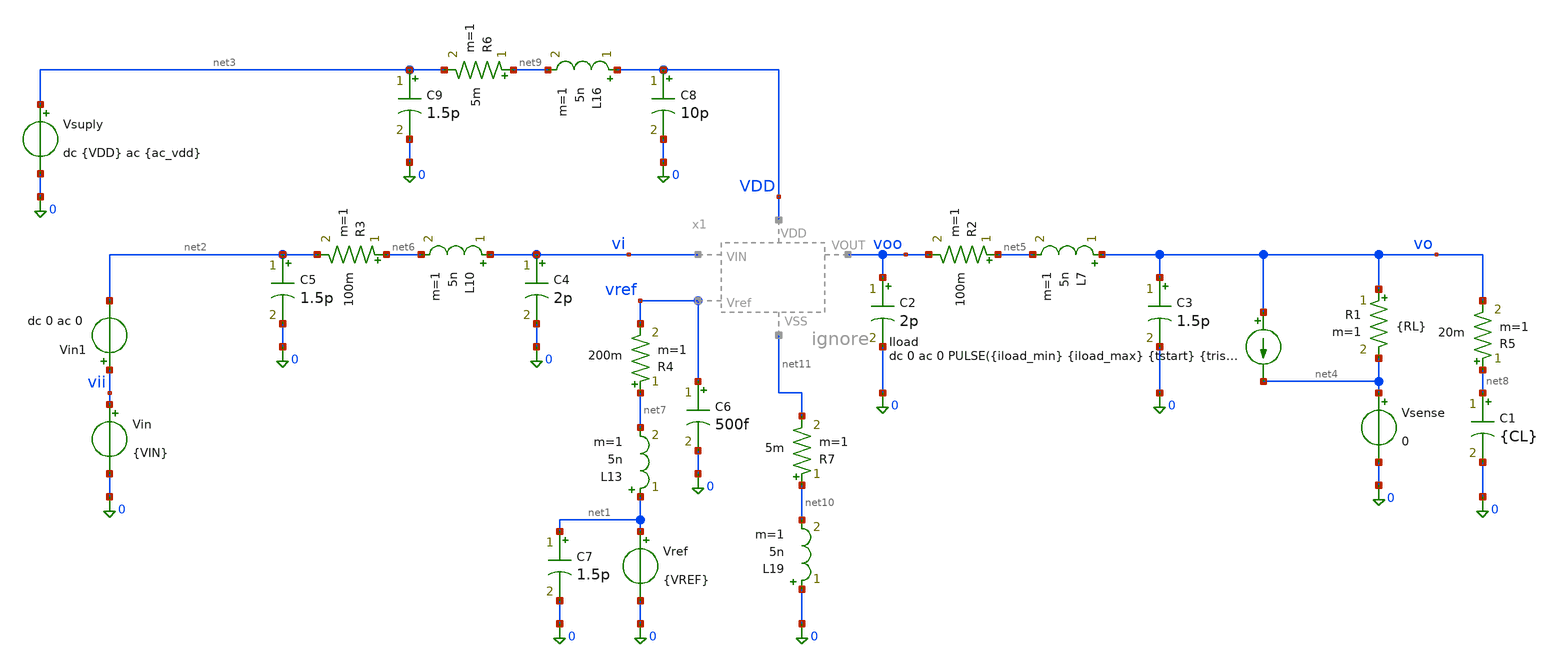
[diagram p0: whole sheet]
** sch_path: xschem/LDO_Top/ldo_tb_pex_montecarlo.sch
**.subckt ldo_tb_pex_montecarlo
Vsuply net3 0 dc {VDD} ac {ac_vdd}
Vref net1 0 {VREF}
Vin vii 0 {VIN}
R1 vo net4 {RL} m=1
C1 net8 0 {CL} m=1
Iload vo net4 dc 0 ac 0 PULSE({iload_min} {iload_max} {tstart} {trise} {tfall} {twidth} {tperiod})
Vsense net4 0 0
Vin1 vii net2 dc 0 ac 0
C2 voo 0 2p m=1
R2 net5 voo 100m m=1
L7 vo net5 5n m=1
C3 vo 0 1.5p m=1
L10 vi net6 5n m=1
C4 vi 0 2p m=1
C5 net2 0 1.5p m=1
R3 net6 net2 100m m=1
L13 net1 net7 5n m=1
R4 net7 vref 200m m=1
C6 vref 0 500f m=1
C7 net1 0 1.5p m=1
R5 net8 vo 20m m=1
L16 VDD net9 5n m=1
C8 VDD 0 10p m=1
C9 net3 0 1.5p m=1
R6 net9 net3 5m m=1
L19 0 net10 5n m=1
R7 net10 net11 5m m=1
**** begin user architecture code


* ==============================================================================
* ENCABEZADO DEL ARCHIVO (ldo_tb_pex_montecarlo.sch):
* Descripción:
*   Banco de pruebas Monte Carlo Post-Layout (PEX) para el regulador LDO
*   completo (incluyendo LDO_pex.spice), incorporando los modelos parásitos de
*   inductancia, resistencia y capacitancia de línea/empaquetado en todos los
*   pines (VIN, VOUT, VDD, Vref, VSS) y la ESR del capacitor de salida.
*   Evalúa Overshoot/Undershoot, PSRR, Line Regulation, Load Regulation y
*   Dropout en cada iteración y guarda en 'datos_mc.txt' con el formato exacto
*   que lee el notebook 'LDO_tb_montecarlo.ipynb'.
* ==============================================================================

* 1. Librería de modelos Sky130 con Mismatch (tt_mm) y netlist PEX del LDO
.lib /foss/pdks/sky130A/libs.tech/ngspice/sky130.lib.spice tt_mm
.include /foss/designs/LDO-sky130/xschem/LDO_Top/LDO_pex.spice
x1 vi voo VDD vref net11 LDO

.option temp=27
.option num_threads=8
.option gmin=1e-12 reltol=1e-3 abstol=1e-12 vntol=1e-6 itl1=500 itl2=200 itl4=100

.param rsh_var = agauss(0, 0.005, 1)

* Guardar únicamente los nodos clave para no desbordar la RAM con la red RC parásita
.save v(vo) v(voo) v(vi) v(vii) v(vdd) v(vref) v(x1.OTA_0.VO_ota) v(x1.OTA_0.VIP_ota) v(x1.self_bias_0.VR)

* Condiciones iniciales en los nodos reales de LDO_pex.spice para convergencia DC
.nodeset V(vo)=1.2
.nodeset V(voo)=1.2
.nodeset V(x1.OTA_0.VIP_ota)=0.6
.nodeset V(x1.OTA_0.VO_ota)=1.1
.nodeset V(x1.self_bias_0.VR)=0.6
.nodeset V(x1.self_bias_0.vgp_self)=1.0

* Parámetros nominales del LDO
.param VDD = 1.8
.param VREF = 0.6
.param VIN = '1*VDD-0.3'
.param RL = 240e9
.param CL = 1u

* Parámetros para la prueba transitoria de carga (Overshoot / Undershoot)
.param iload_min = 1u
.param iload_max = 5m
.param tstart   = 30u
.param trise    = 100n
.param tfall    = 100n
.param twidth   = 100u
.param tperiod  = 200u
.param tsim     = '2*tperiod'

.param ac_iprobe = 0
.param ac_vdd    = 0

* --- Clamp SOLO de simulación (evita soluciones DC falsas en los nodos reales del PEX) ---
Dclpn 0 vo dclamp_tb
Dclpp vo vclp dclamp_tb
Dclpn2 0 x1.OTA_0.VIP_ota dclamp_tb
Dclpp2 x1.OTA_0.VIP_ota vclp dclamp_tb
Vclp vclp 0 5
.model dclamp_tb D(IS=1e-15 N=1)

.control
* =========================================================
* CONFIGURACION DEL BUCLE MONTE CARLO PEX
* =========================================================
let mc_runs = 100
let run = 1

set appendwrite
set filetype=ascii

let tperiod = 200u
let tsim = 2 * tperiod

echo === INICIO MONTE CARLO PEX === > datos_mc.txt

* =========================================================
* INICIO DEL BUCLE MONTE CARLO PEX
* =========================================================
while run <= mc_runs

    echo ======================================
    echo CORRIENDO MONTE CARLO PEX ITERACION: $&run
    echo ======================================
    echo --- ITERACION: $&run --- >> datos_mc.txt

    * En la iteración 1 el circuito ya fue cargado con su primera semilla;
    * a partir de la iteración 2 hacemos UN SOLO 'reset' por chip para
    * sortear nuevos parámetros estadísticos (agauss) y restaurar las fuentes.
    if run > 1
        reset
    end

    save v(vo) v(vi) v(vdd)

    * -----------------------------------------------------
    * A. TRANSIENTE (Overshoot y Undershoot)
    * -----------------------------------------------------
    tran 5u $&tsim

    let t_ignorar = 150u
    meas tran v_estable_ligera FIND v(vo) AT=270u
    meas tran v_estable_pesada FIND v(vo) AT=180u
    meas tran vo_max MAX v(vo) from=$&t_ignorar to=$&tsim
    meas tran vo_min MIN v(vo) from=$&t_ignorar to=$&tsim
    meas tran salida_tran avg v(vo) from=$&t_ignorar to=$&tsim

    let undershoot_mV = (v_estable_ligera - vo_min) * 1e3
    let overshoot_mV  = (vo_max - v_estable_pesada) * 1e3

    echo 'undershoot_mV = $&undershoot_mV' >> datos_mc.txt
    echo 'overshoot_mV = $&overshoot_mV' >> datos_mc.txt
    echo 'salida_tran = $&salida_tran' >> datos_mc.txt

    * -----------------------------------------------------
    * B. AC (PSRR)
    * -----------------------------------------------------
    * Usamos 'alter' en lugar de 'alterparam + reset' para no recargar
    * el netlist PEX ni cambiar la semilla aleatoria del chip actual.
    alter @Vsuply[acmag] = 1

    ac dec 10 10 1G
    let psrr1 = v(vdd)/v(vo)
    let psrr_db = vdb(psrr1)

    meas ac gananciaPSRR_1   find psrr_db at=10
    meas ac gananciaPSRR_1k  find psrr_db at=1k
    meas ac gananciaPSRR_10k find psrr_db at=10k
    meas ac gananciaPSRR_1M  find psrr_db at=1Meg

    echo 'psrr_1 = $&gananciaPSRR_1' >> datos_mc.txt
    echo 'psrr_1k = $&gananciaPSRR_1k' >> datos_mc.txt
    echo 'psrr_10k = $&gananciaPSRR_10k' >> datos_mc.txt
    echo 'psrr_1M = $&gananciaPSRR_1M' >> datos_mc.txt

    alter @Vsuply[acmag] = 0

    * -----------------------------------------------------
    * C. TRANSIENTE (Line Regulation)
    * -----------------------------------------------------
    alter @Vin[pwl] = [ 0 1.4 1m 1.8 ]
    alter @Iload[pwl] = [ 0 1u 1m 1u ]

    tran 20u 1m

    let t_line_ini = 40u
    let t_line_fin = 950u

    meas tran voline_max MAX v(vo) from=$&t_line_ini to=$&t_line_fin
    meas tran voline_min MIN v(vo) from=$&t_line_ini to=$&t_line_fin
    meas tran salida_line avg v(vo) from=$&t_line_ini to=$&t_line_fin
    let line_regulation_mV = (voline_max - voline_min) * 1000

    echo 'line_regulation_mv = $&line_regulation_mV' >> datos_mc.txt
    echo 'salida_line = $&salida_line' >> datos_mc.txt

    * -----------------------------------------------------
    * D. TRANSIENTE (Load Regulation)
    * -----------------------------------------------------
    alter @Vin[pwl] = [ 0 1.5 1m 1.5 ]
    alter @Iload[pwl] = [ 0 1u 1m 5m ]

    tran 20u 1m

    meas tran vout_light FIND v(vo) AT=40u
    meas tran vout_heavy FIND v(vo) AT=1m

    let load_regulation_mV = (vout_light - vout_heavy) * 1000

    echo 'load_regulation_mV = $&load_regulation_mV' >> datos_mc.txt

    * -----------------------------------------------------
    * E. TRANSIENTE (Dropout)
    * -----------------------------------------------------
    alter r1 = 240
    alter @Vin[pwl] = [ 0 2 1m 0 ]
    alter @Iload[pwl] = [ 0 1u 1m 1u ]

    tran 20u 1m

    meas tran vout_nom FIND v(vo) AT=225u
    let vout_target = vout_nom * 0.90

    meas tran vin_do FIND v(vi) WHEN v(vo) = vout_target fall=1
    let dropout_mV = (vin_do - vout_target) * 1e3

    echo 'dropout_mV = $&dropout_mV' >> datos_mc.txt

    * -----------------------------------------------------
    * Liberar los vectores de memoria RAM al terminar la iteración
    * -----------------------------------------------------
    destroy all

    let run = run + 1

end

echo === FIN MONTE CARLO PEX === >> datos_mc.txt
echo ======================================
echo SIMULACION MONTE CARLO PEX FINALIZADA
echo ======================================
.endc


**** end user architecture code
**.ends
.end
